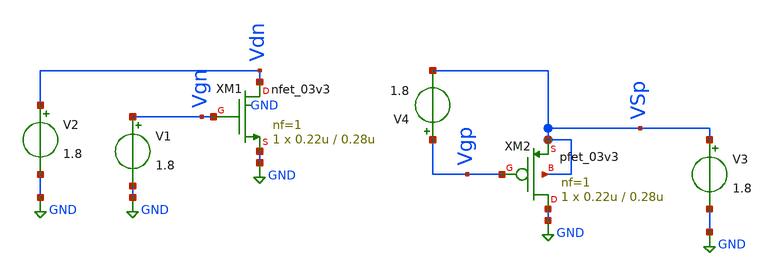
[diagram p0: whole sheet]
** sch_path: xschem/caracterizador/charac.sch
* Copyright 2022 GlobalFoundries PDK Authors
* Licensed under the Apache License, Version 2.0 (the "License");
* you may not use this file except in compliance with the License.
* You may obtain a copy of the License at
* https://www.apache.org/licenses/LICENSE-2.0
* Unless required by applicable law or agreed to in writing, software
* distributed under the License is distributed on an "AS IS" BASIS,
* WITHOUT WARRANTIES OR CONDITIONS OF ANY KIND, either express or implied.
* See the License for the specific language governing permissions and
* limitations under the License.
**.subckt charac
XM1 Vdn Vgn GND GND nfet_03v3 L=0.28u W=0.22u nf=1 ad='int((nf+1)/2) * W/nf * 0.18u' as='int((nf+2)/2) * W/nf * 0.18u'
+ pd='2*int((nf+1)/2) * (W/nf + 0.18u)' ps='2*int((nf+2)/2) * (W/nf + 0.18u)' nrd='0.18u / W' nrs='0.18u / W'
+ sa=0 sb=0 sd=0 m=1 par=1
XM2 GND Vgp VSp VSp pfet_03v3 L=0.28u W=0.22u nf=1 ad='int((nf+1)/2) * W/nf * 0.18u' as='int((nf+2)/2) * W/nf * 0.18u'
+ pd='2*int((nf+1)/2) * (W/nf + 0.18u)' ps='2*int((nf+2)/2) * (W/nf + 0.18u)' nrd='0.18u / W' nrs='0.18u / W'
+ sa=0 sb=0 sd=0 m=1 par=1
V1 Vgn GND 1.8
V2 Vdn GND 1.8
V3 VSp GND 1.8
V4 Vgp VSp 1.8
**** begin user architecture code



.control
  save all

* ======================= CONFIGURACIÓN PERSONALIZADA DE COLORES Y ESTILO ========================
set color0=white * Fondo blanco (o 'black' si prefieres fondo oscuro) [1, 2]
set color1=black * Texto y rejilla negros (si el fondo es blanco) [1, 2]
set color2=red * 1ª curva
set color3=blue * 2ª curva
set color4=green * 3ª curva
set color5=magenta * 4ª curva
set color6=cyan * 5ª curva
set color7=orange * 6ª curva
set color8=darkgreen * 7ª curva
set xbrushwidth=2 * Hace el trazo de las curvas más grueso y visible [2, 4]

  * ===== NMOS =====
  dc V2 0 3.3 0.01 V1 0 3.3 0.55
  plot -i(V2) title 'NMOS Output' xlabel 'VDS' ylabel 'ID'

  dc V1 0 3.3 0.01 V2 0.55 3.3 0.55
  plot -i(V2) title 'NMOS Transfer' xlabel 'VGS' ylabel 'ID'

  alter V2 = 1.65
  dc V1 0 3.3 0.01
  let idn = -i(V2)
  let gmn = deriv(idn)
  let gmidn = gmn/idn
  plot gmidn vs idn xlog xlimit 1e-9 1e-3 ylimit 0 35 title 'NMOS gm/Id' xlabel 'ID' ylabel 'gm/ID (1/V)'

  * ===== PMOS (V3 = VSD, V4 = VGS negativo, referido a la fuente) =====
  dc V3 0 3.3 0.01 V4 0 -3.3 -0.55
  plot -i(V3) title 'PMOS Output' xlabel 'VSD' ylabel '|ID|'

  dc V4 0 -3.3 -0.01 V3 0.55 3.3 0.55
  plot -i(V3) title 'PMOS Transfer' xlabel 'VGS' ylabel '|ID|'

  alter V3 = 1.65
  dc V4 0 -3.3 -0.01
  let idp = -i(V3)
  let gmp = abs(deriv(idp))
  let gmidp = gmp/idp
  plot gmidp vs idp xlog xlimit 1e-9 1e-3 ylimit 0 35 title 'PMOS gm/Id' xlabel '|ID| (A)' ylabel 'gm/ID (1/V)'
.endc




.include /home/ringosinye/eda/pdks/gf180mcuD/libs.tech/ngspice/design.ngspice
.lib /home/ringosinye/eda/pdks/gf180mcuD/libs.tech/ngspice/sm141064.ngspice typical
.param sw_stat_mismatch = 0




.control
save all

* Coloracion de graficas
set color0=white
set color1=black
set color2=blue
set xbrushwidth=2

* ========================================================
* 1. CARACTERIZACION NMOS (Voltaje fijo VDS = 1.65 V)
* ========================================================
alter V2 = 1.65
dc V1 0 3.3 0.01

let idn = abs(-i(V2)) + 1e-15
let gmn = deriv(idn)
let gmidn = gmn/idn

* --- MEDICIONES AUTOMATICAS NMOS ---
meas dc vth_n find v(vgn) when idn=100n
meas dc gmn_max max gmn
meas dc id_inv_mod_n find idn when gmidn=15

* Guardar valores numéricos en variables antes de cambiar de simulación
set vth_n_val = $&vth_n
set gmn_val = $&gmn_max
set id_mod_n_val = $&id_inv_mod_n

* ========================================================
* 2. RESISTENCIA DE SALIDA NMOS (ro) en VGS = 1.65 V
* ========================================================
alter V1 = 1.65
dc V2 0 3.3 0.01

let idn_sat = abs(-i(V2))
let gds_n_vec = deriv(idn_sat)
meas dc gds_n find gds_n_vec at=1.65

set gds_n_val = $&gds_n
let ro_n = 1 / gds_n
let av_n = $gmn_val * ro_n

set ro_n_val = $&ro_n
set av_n_val = $&av_n

* ========================================================
* 1. CARACTERIZACION PMOS (Voltaje fijo VSD = 1.65 V)
* ========================================================
alter V3 = 1.65
dc V4 0 -3.3 -0.01

let idp = abs(i(V3)) + 1e-15
let gmp = abs(deriv(idp))
let gmidp = gmp/idp
let vgsp = vgp-vsp

* --- MEDICIONES AUTOMATICAS PMOS ---
meas dc vth_p find vgsp when idp=100n
meas dc gmp_max max gmp
meas dc id_inv_mod_p find idp when gmidp=15

* Guardar valores numéricos en variables antes de cambiar de simulación
set vth_p_val = $&vth_p
set gmp_val = $&gmp_max
set id_mod_p_val = $&id_inv_mod_p

* ========================================================
* 2. RESISTENCIA DE SALIDA NMOS (ro) en VSG= 1.65 V
* ========================================================
alter V4 = -1.65
dc V3 0 3.3 0.01

let idp_sat = abs(i(V3))
let gds_p_vec = deriv(idp_sat)
meas dc gds_p find gds_p_vec at=1.65

set gds_p_val = $&gds_p
let ro_p = 1 / gds_p
let av_p = $gmp_val * ro_p

set ro_p_val = $&ro_p
set av_p_val = $&av_p


* --- IMPRIMIR RESULTADOS EN CONSOLA ---
echo ================ RESUMEN NMOS ================
echo Vth_n = $vth_n_val V
echo gmn_max = $gmn_val S
echo ID_inv_mod_n = $id_mod_n_val A
echo gds_n = $gds_n_val S
echo ro_n = $ro_n_val Ohms
echo Av_n (gmn*ron) = $av_n_val V/V
echo ==============================================
echo ================ RESUMEN PMOS ================
echo Vth_p = $vth_p_val V
echo gmp_max = $gmp_val S
echo ID_inv_mod_p = $id_mod_p_val A
echo gds_p = $gds_p_val S
echo ro_p = $ro_p_val Ohms
echo Av_p (gmp*rop) = $av_p_val V/V
echo ==============================================
.endc




.control
    save all

    * Coloracion de graficas
    set color0=white
    set color1=black
    set color2=blue
    set color3=red
    set xbrushwidth=2

    * ========================================================
    * 1. MEDIDA DE fT PARA NMOS (VDS = 1.65V, VGS = 1.65V)
    * ========================================================
    alter V2 = 1.65
    alter V1 = 1.65
    alter V1 acmag = 1

    * Analisis AC de 1 kHz a 100 GHz (20 puntos por decada)
    ac dec 20 1k 100G

    * Ganancia de corriente H21 = i(V2) / i(V1)
    let h21_n = abs(i(V2) / i(V1))

    * Medir la frecuencia cuando H21 cae a 1 (0 dB)
    meas ac fT_n when h21_n=1


    * ========================================================
    * 2. MEDIDA DE fT PARA PMOS (VSD = 1.65V, VGS = -1.65V)
    * ========================================================
    alter V3 = 1.65
    alter V4 = -1.65
    alter V4 acmag = 1

    ac dec 20 1k 100G
    let h21_p = abs(i(V3) / i(V4))
    meas ac fT_p when h21_p=1


* Graficar ganancia de corriente en dB vs Frecuencia
    plot db(ac1.h21_n) db(ac2.h21_p) xlog title 'Ganancia de Corriente H21 (fT)' xlabel 'Frecuencia (Hz)'
+ ylabel 'H21 (dB)'

    * --- IMPRIMIR RESULTADOS EN CONSOLA ---
    echo ================ RESULTADOS AC (fT) ================
    print ac1.fT_n ac2.fT_p
    echo ====================================================

.endc




.control
  save all

  * Coloración de gráficas
  set color0 = white
  set color1 = black
  set color2 = blue
  set color3 = red
  set xbrushwidth = 2

  * ========================================================
  * 1. CAPACITANCIA DE COMPUERTA NMOS (VDS = 1.65V, VGS = 1.65V)
  * ========================================================
  alter V2 = 1.65
  alter V1 = 1.65
  alter V1 acmag = 1

  * Barrido AC de 1 kHz a 100 MHz (1 MHz queda holgadamente dentro)
  ac dec 10 1k 100M
  let cgg_n = imag(-i(V1)) / (2 * pi * frequency)
  meas ac cgg_n_val find cgg_n at = 1meg

  * ========================================================
  * 2. CAPACITANCIA DE COMPUERTA PMOS (VSD = 1.65V, VGS = -1.65V)
  * ========================================================
  alter V3 = 1.65
  alter V4 = -1.65
  alter V4 acmag = 1

  ac dec 10 1k 100M
  let cgg_p = imag(-i(V4)) / (2 * pi * frequency)
  meas ac cgg_p_val find cgg_p at = 1meg

* --- GRAFICAR CAPACITANCIAS VS FRECUENCIA ---
plot ac1.cgg_n ac2.cgg_p xlog title 'Capacitancia de Compuerta Cgg vs Frecuencia' xlabel 'Frecuencia (Hz)'
+ ylabel 'Cgg (F)'

  * --- IMPRIMIR CAPACITANCIAS ---
  echo ================ CAPACITANCIAS DE COMPUERTA (Cgg @ 1MHz) ================
  print ac1.cgg_n_val ac2.cgg_p_val
  echo =========================================================================
.endc


**** end user architecture code
**.ends
.GLOBAL GND
.end
